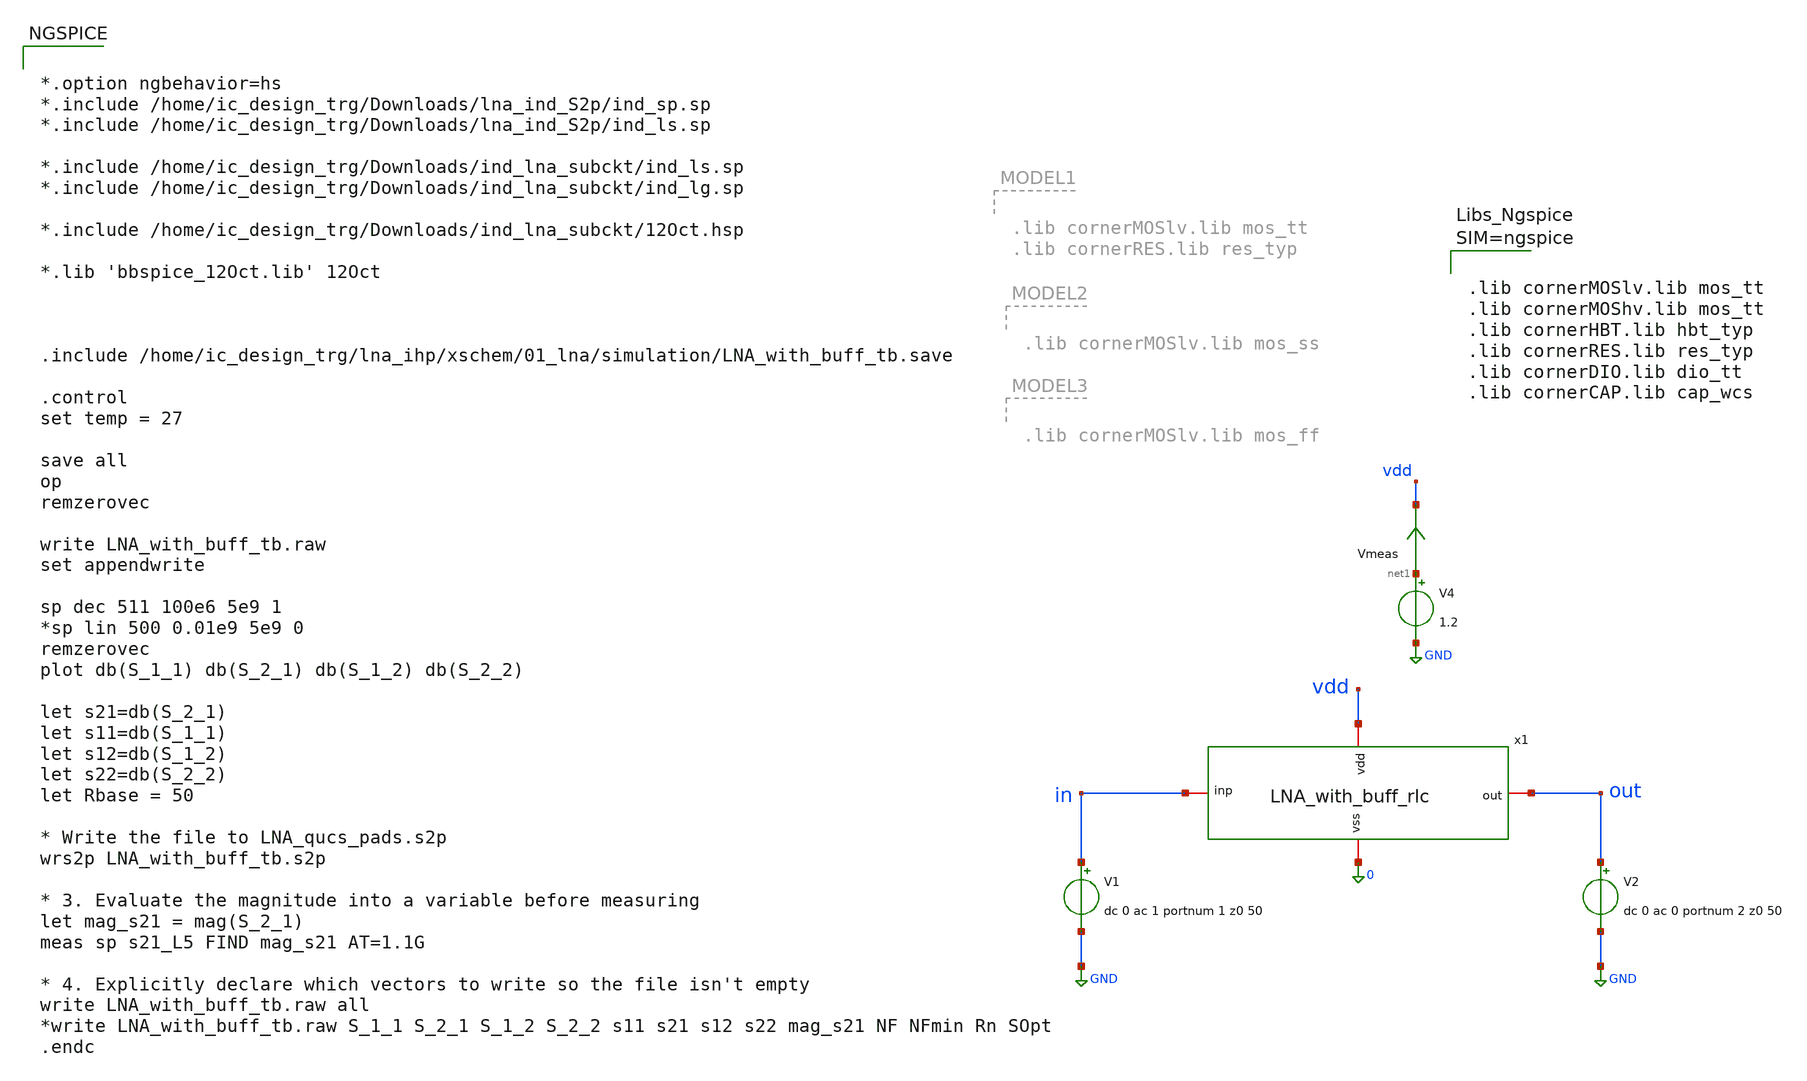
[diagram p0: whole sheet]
** sch_path: LNA7096-main/schematic/xschem/01_lna/LNA_with_buff_tb.sch
**.subckt LNA_with_buff_tb
V1 in GND dc 0 ac 1 portnum 1 z0 50
V2 out GND dc 0 ac 0 portnum 2 z0 50
V4 net1 GND 1.2
Vmeas net1 vdd 0
.save i(vmeas)
x1 vdd out in 0 LNA_with_buff_rlc
**** begin user architecture code


*.option ngbehavior=hs
*.include /home/ic_design_trg/Downloads/lna_ind_S2p/ind_sp.sp
*.include /home/ic_design_trg/Downloads/lna_ind_S2p/ind_ls.sp

*.include /home/ic_design_trg/Downloads/ind_lna_subckt/ind_ls.sp
*.include /home/ic_design_trg/Downloads/ind_lna_subckt/ind_lg.sp

*.include /home/ic_design_trg/Downloads/ind_lna_subckt/12Oct.hsp

*.lib 'bbspice_12Oct.lib' 12Oct



.include /home/ic_design_trg/lna_ihp/xschem/01_lna/simulation/LNA_with_buff_tb.save

.control
set temp = 27

save all
op
remzerovec

write LNA_with_buff_tb.raw
set appendwrite

sp dec 511 100e6 5e9 1
*sp lin 500 0.01e9 5e9 0
remzerovec
plot db(S_1_1) db(S_2_1) db(S_1_2) db(S_2_2)

let s21=db(S_2_1)
let s11=db(S_1_1)
let s12=db(S_1_2)
let s22=db(S_2_2)
let Rbase = 50

* Write the file to LNA_qucs_pads.s2p
wrs2p LNA_with_buff_tb.s2p

* 3. Evaluate the magnitude into a variable before measuring
let mag_s21 = mag(S_2_1)
meas sp s21_L5 FIND mag_s21 AT=1.1G

* 4. Explicitly declare which vectors to write so the file isn't empty
write LNA_with_buff_tb.raw all
*write LNA_with_buff_tb.raw S_1_1 S_2_1 S_1_2 S_2_2 s11 s21 s12 s22 mag_s21 NF NFmin Rn SOpt
.endc





.lib cornerMOSlv.lib mos_tt
.lib cornerMOShv.lib mos_tt
.lib cornerHBT.lib hbt_typ
.lib cornerRES.lib res_typ
.lib cornerDIO.lib dio_tt
.lib cornerCAP.lib cap_wcs



**** end user architecture code
**.ends

* expanding   symbol:  01_lna/LNA_with_buff_rlc.sym # of pins=4
** sym_path: LNA7096-main/schematic/xschem/01_lna/LNA_with_buff_rlc.sym
** sch_path: LNA7096-main/schematic/xschem/01_lna/LNA_with_buff_rlc.sch
.subckt LNA_with_buff_rlc vdd out inp vss
*.iopin vdd
*.iopin vss
*.iopin inp
*.iopin out
XR1 n5 vss vss rhigh w=1e-6 l=21.44e-6 m=1 b=1 mm_ok=1
XR2 vdd n5 vss rhigh w=1e-6 l=5e-6 m=1 b=0 mm_ok=1
XR3 vdd n8 vss rhigh w=1e-6 l=5e-6 m=1 b=0 mm_ok=1
XR4 bias n4 vss rhigh w=1e-6 l=10e-6 m=1 b=0 mm_ok=1
XR5 vdd bias vss rhigh w=1e-6 l=7e-6 m=1 b=0 mm_ok=1
XC1 n1 n5 vss cap_rfcmim w=58e-6 l=59e-6 wfeed=5.0e-6 m=1 mm_ok=1
XC3 n6 out vss cap_rfcmim w=58e-6 l=57.5e-6 wfeed=5.0e-6 m=1 mm_ok=1
XC2 inp n4 vss cap_rfcmim w=64.6e-6 l=62e-6 wfeed=5.0e-6 m=1 mm_ok=1
XC4 n6 out vss cap_rfcmim w=58e-6 l=57.5e-6 wfeed=5.0e-6 m=1 mm_ok=1
XM5 n1 vdd n9 vss sg13_lv_nmos w=410u l=0.25u ng=82 m=1 rfmode=1 mm_ok=1
XM3 n9 n3 n2 vss sg13_lv_nmos w=410u l=0.25u ng=82 m=1 rfmode=1 mm_ok=1
XM2 n8 n8 vss vss sg13_lv_nmos w=5u l=0.25u ng=1 m=1 rfmode=1 mm_ok=1
XM4 n6 n8 vss vss sg13_lv_nmos w=86u l=0.25u ng=35 m=1 rfmode=1 mm_ok=1
XM1 vdd n5 n6 n6 sg13_lv_nmos w=160u l=0.25u ng=20 m=1 rfmode=1 mm_ok=1
XM6 bias bias vss vss sg13_lv_nmos w=5u l=0.25u ng=1 m=1 rfmode=1 mm_ok=1
x2 n4 n3 net2 ind_rlc Lser=18.1n Rser=9.8 Cshunt1=61.6f Rshunt1=2696 Cshunt2=62.2f Rshunt2=2774
XL6 vdd n1 vss 12_oct_t-4_w-14_s-2_dia-469_gds
XL4 n2 vss vss 13_oct_t-2_w-15_s-2_dia-168
XD1 n6 vdd vss isolbox l=29.14u w=10.735u
.ends


* expanding   symbol:  01_lna/ind_rlc.sym # of pins=3
** sym_path: LNA7096-main/schematic/xschem/01_lna/ind_rlc.sym
** sch_path: LNA7096-main/schematic/xschem/01_lna/ind_rlc.sch
.subckt ind_rlc p2 p1 vss  Lser=1n Rser=1k Rshunt1=1k Cshunt1=2p Rshunt2=1k Cshunt2=2p
*.iopin p1
*.iopin p2
*.iopin vss
L1 net2 p1 'Lser' m=1
R1 net2 p2 'Rser' m=1
R2 p1 net1 'Rshunt1' m=1
C1 net1 vss 'Cshunt1' m=1
R5 p2 net3 'Rshunt2' m=1
C4 net3 vss 'Cshunt2' m=1
.ends


* expanding   symbol:  01_lna/12_oct_t-4_w-14_s-2_dia-469_gds.sym # of pins=3
** sym_path: LNA7096-main/schematic/xschem/01_lna/ind_lg.sym
.include /home/ic_design_trg/lna_ihp/xschem/01_lna/lna_pads/simulation/ngspice_s2p/12_oct_t-4_w-14_s-2_dia-469_gds.inc

* expanding   symbol:  01_lna/13_oct_t-2_w-15_s-2_dia-168.sym # of pins=3
** sym_path: LNA7096-main/schematic/xschem/01_lna/ind_lg.sym
.include /home/ic_design_trg/lna_ihp/xschem/01_lna/lna_pads/simulation/ngspice_s2p/13_oct_t-2_w-15_s-2_dia-168.inc
.GLOBAL GND
.end
